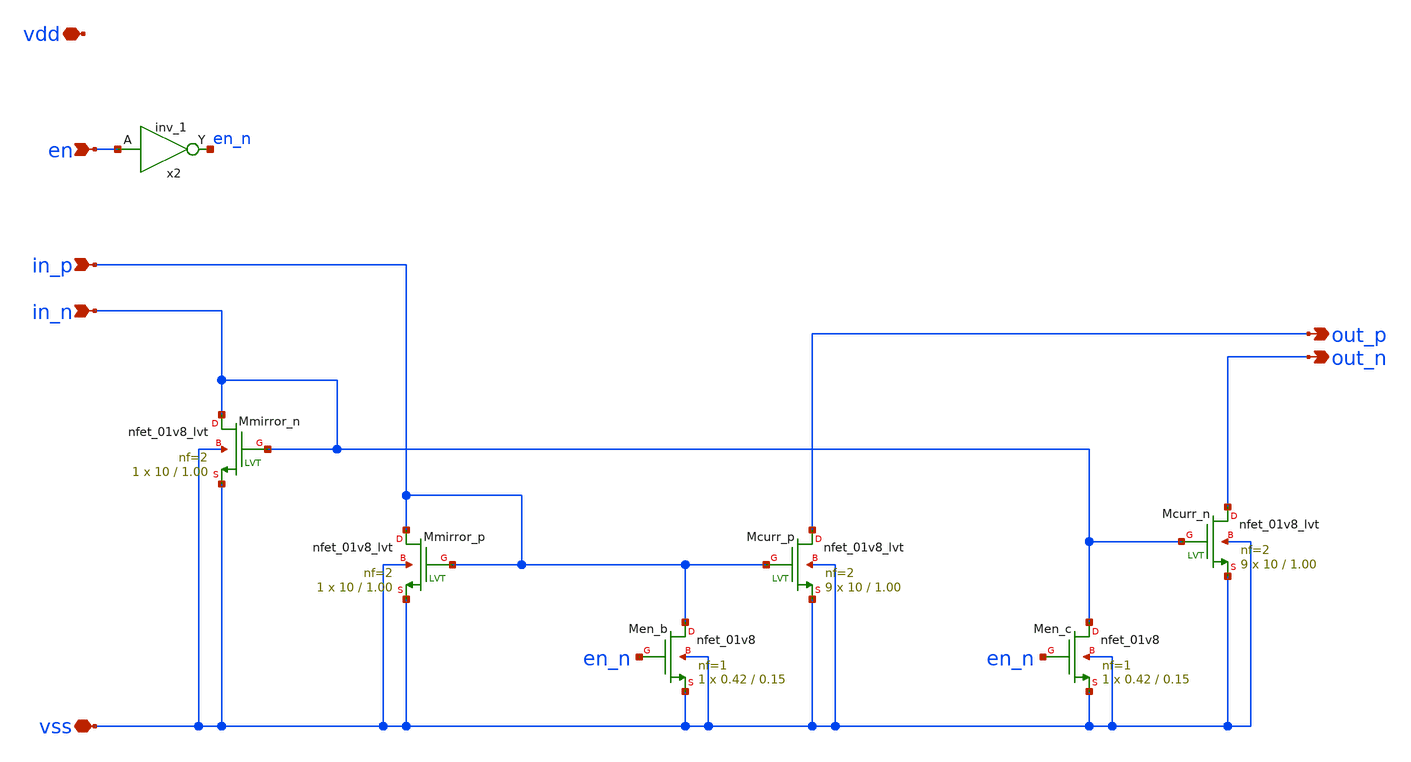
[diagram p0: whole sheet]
** sch_path: xschem/dac_curr_mult/dac_curr_mult.sch
**.subckt dac_curr_mult in_n in_p vss vdd out_p out_n en
*.ipin in_n
*.ipin in_p
*.iopin vss
*.iopin vdd
*.opin out_p
*.opin out_n
*.ipin en
XMcurr_p out_p in_p vss vss sky130_fd_pr__nfet_01v8_lvt L=1.00 W=10 nf=2 ad='int((nf+1)/2) * W/nf * 0.29'
+ as='int((nf+2)/2) * W/nf * 0.29' pd='2*int((nf+1)/2) * (W/nf + 0.29)' ps='2*int((nf+2)/2) * (W/nf + 0.29)'
+ nrd='0.29 / W' nrs='0.29 / W' sa=0 sb=0 sd=0 mult=9 m=9
XMcurr_n out_n in_n vss vss sky130_fd_pr__nfet_01v8_lvt L=1.00 W=10 nf=2 ad='int((nf+1)/2) * W/nf * 0.29'
+ as='int((nf+2)/2) * W/nf * 0.29' pd='2*int((nf+1)/2) * (W/nf + 0.29)' ps='2*int((nf+2)/2) * (W/nf + 0.29)'
+ nrd='0.29 / W' nrs='0.29 / W' sa=0 sb=0 sd=0 mult=9 m=9
XMmirror_n in_n in_n vss vss sky130_fd_pr__nfet_01v8_lvt L=1.00 W=10 nf=2 ad='int((nf+1)/2) * W/nf * 0.29'
+ as='int((nf+2)/2) * W/nf * 0.29' pd='2*int((nf+1)/2) * (W/nf + 0.29)' ps='2*int((nf+2)/2) * (W/nf + 0.29)'
+ nrd='0.29 / W' nrs='0.29 / W' sa=0 sb=0 sd=0 mult=1 m=1
XMmirror_p in_p in_p vss vss sky130_fd_pr__nfet_01v8_lvt L=1.00 W=10 nf=2 ad='int((nf+1)/2) * W/nf * 0.29'
+ as='int((nf+2)/2) * W/nf * 0.29' pd='2*int((nf+1)/2) * (W/nf + 0.29)' ps='2*int((nf+2)/2) * (W/nf + 0.29)'
+ nrd='0.29 / W' nrs='0.29 / W' sa=0 sb=0 sd=0 mult=1 m=1
XMen_b in_p en_n vss vss sky130_fd_pr__nfet_01v8 L=0.15 W=0.42 nf=1 ad='int((nf+1)/2) * W/nf * 0.29'
+ as='int((nf+2)/2) * W/nf * 0.29' pd='2*int((nf+1)/2) * (W/nf + 0.29)' ps='2*int((nf+2)/2) * (W/nf + 0.29)'
+ nrd='0.29 / W' nrs='0.29 / W' sa=0 sb=0 sd=0 mult=1 m=1
XMen_c in_n en_n vss vss sky130_fd_pr__nfet_01v8 L=0.15 W=0.42 nf=1 ad='int((nf+1)/2) * W/nf * 0.29'
+ as='int((nf+2)/2) * W/nf * 0.29' pd='2*int((nf+1)/2) * (W/nf + 0.29)' ps='2*int((nf+2)/2) * (W/nf + 0.29)'
+ nrd='0.29 / W' nrs='0.29 / W' sa=0 sb=0 sd=0 mult=1 m=1
x2 en vss vss vdd vdd en_n sky130_fd_sc_hs__inv_1
**.ends
.end
